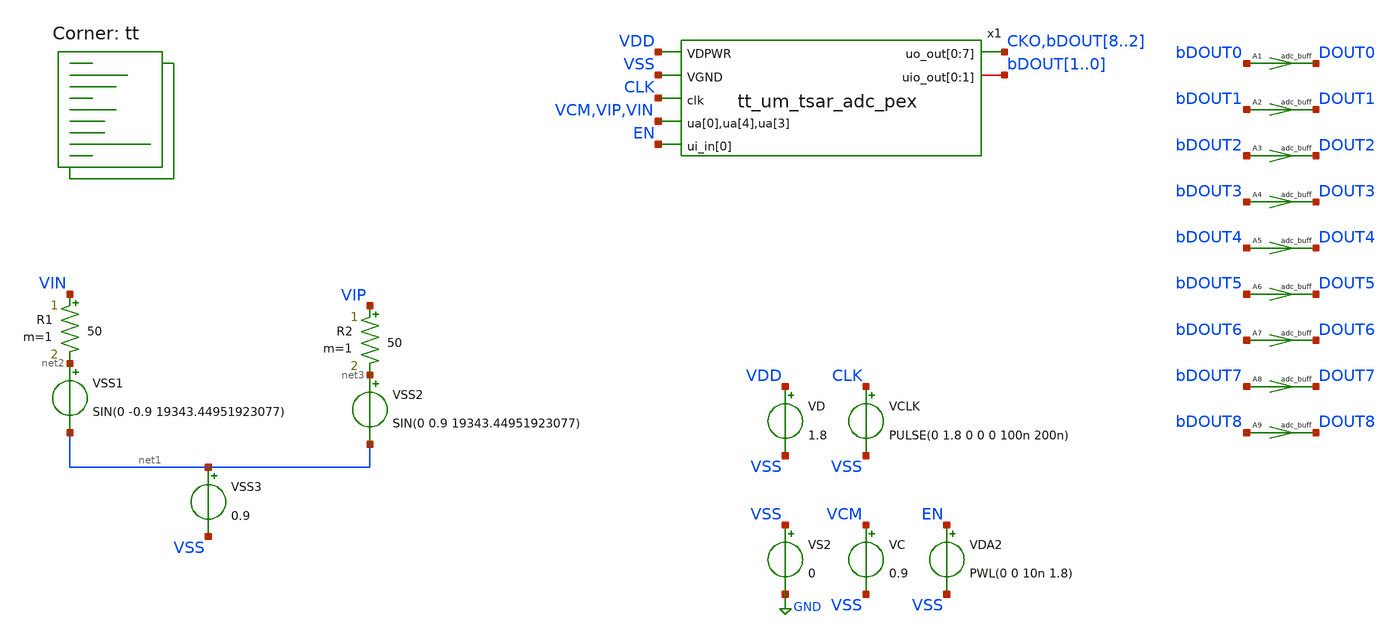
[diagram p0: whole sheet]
** sch_path: xschem/adc_tb.sch
**.subckt adc_tb
VSS1 net2 net1 SIN(0 -0.9 19343.44951923077)
VSS2 net3 net1 SIN(0 0.9 19343.44951923077)
VSS3 net1 VSS 0.9
VCLK CLK VSS PULSE(0 1.8 0 0 0 100n 200n)
R1 VIN net2 50 m=1
R2 VIP net3 50 m=1
VC VCM VSS 0.9
VDA2 EN VSS PWL(0 0 10n 1.8)
A1 [ bDOUT0 ] [ DOUT0 ] adc_buff
A2 [ bDOUT1 ] [ DOUT1 ] adc_buff
A3 [ bDOUT2 ] [ DOUT2 ] adc_buff
A4 [ bDOUT3 ] [ DOUT3 ] adc_buff
A5 [ bDOUT4 ] [ DOUT4 ] adc_buff
A6 [ bDOUT5 ] [ DOUT5 ] adc_buff
A7 [ bDOUT6 ] [ DOUT6 ] adc_buff
A8 [ bDOUT7 ] [ DOUT7 ] adc_buff
VS2 VSS GND 0
VD VDD VSS 1.8
A9 [ bDOUT8 ] [ DOUT8 ] adc_buff
x1 VDD VSS CLK CKO bDOUT8 bDOUT7 bDOUT6 bDOUT5 bDOUT4 bDOUT3 bDOUT2 bDOUT1 bDOUT0 VCM VIP VIN EN
+ tt_um_tsar_adc_pex
**** begin user architecture code

** opencircuitdesign pdks install
* .lib $::SKYWATER_MODELS/sky130.lib.spice tt
*.include $PDK_ROOT/$PDK/libs.ref/sky130_fd_sc_hdll/spice/sky130_fd_sc_hdll.spice
.include $PDK_ROOT/$PDK/libs.ref/sky130_fd_sc_hs/spice/sky130_fd_sc_hs.spice
.include $PDK_ROOT/$PDK/libs.ref/sky130_fd_sc_hd/spice/sky130_fd_sc_hd.spice



.option wnflag=0 bypass=1
.options method=trap rawfile=binary
.options solver=klu nomod
Eout out 0 VALUE = { ((V(dout0)*256 + V(dout1)*128 + V(dout2)*64 + V(dout3)*32 + V(dout4)*16 + V(dout5)*8 + V(dout6)*4 + V(dout7)*2 + V(dout8)*1)/3.3) - 256 }
Epowa pow 0 VALUE = { V(vdd)*(-i(vd)) }
.model adc_buff adc_bridge(in_low=0.18 in_high=1.62 rise_delay=100p fall_delay=100p)
.control
global netlist_dir .
set num_threads=16
save cko out pow vip vin x1.vcp x1.vcn 'x1.cf[0]' 'x1.cf[1]' 'x1.cf[2]' 'x1.cf[3]' 'x1.cf[4]' 'x1.cf[5]'
+ 'x1.cf[6]' 'x1.cf[7]' 'x1.cf[8]'
tran 10n 5350u 0 ; Mengubah start time menjadi 10n
rusage traniter trantime
meas tran avg_pow  AVG pow from=1n to=535u
remzerovec
write adc8b_tb_dynamic.raw
wrdata adc8b_tb_dynamic.txt out cko pow_a pow_d pow_r vip vin
quit 1
.endc


.lib $::SKYWATER_MODELS/sky130.lib.spice tt
**** end user architecture code
**.ends

* expanding   symbol:  tt_um_tsar_adc_pex.sym # of pins=7
** sym_path: xschem/tt_um_tsar_adc_pex.sym
.include /home/huda/ITS_Analog_10b_TADC/mag/tt_um_tsar_adc_pex.spice
.GLOBAL GND
.end
